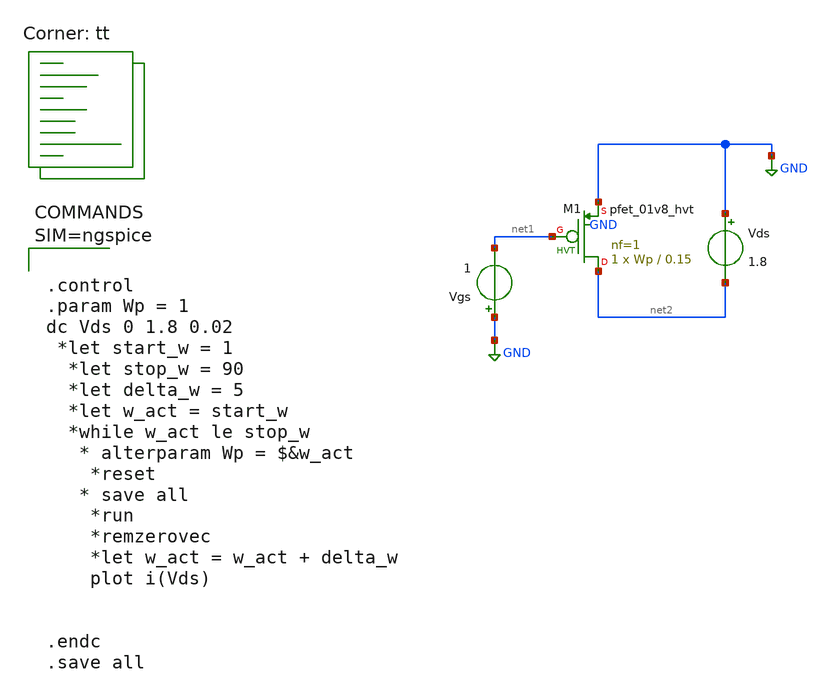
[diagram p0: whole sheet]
** sch_path: xschem/Polarizzazione0.sch
**.subckt Polarizzazione0
Vgs GND net1 1
Vds GND net2 1.8
XM1 net2 net1 GND GND sky130_fd_pr__pfet_01v8_hvt L=0.15 W=Wp nf=1 ad='int((nf+1)/2) * W/nf * 0.29' as='int((nf+2)/2) * W/nf * 0.29'
+ pd='2*int((nf+1)/2) * (W/nf + 0.29)' ps='2*int((nf+2)/2) * (W/nf + 0.29)' nrd='0.29 / W' nrs='0.29 / W'
+ sa=0 sb=0 sd=0 mult=1 m=1
**** begin user architecture code
.lib $::SKYWATER_MODELS/sky130.lib.spice tt



.control
.param Wp = 1
dc Vds 0 1.8 0.02
 *let start_w = 1
  *let stop_w = 90
  *let delta_w = 5
  *let w_act = start_w
  *while w_act le stop_w
   * alterparam Wp = $&w_act
    *reset
   * save all
    *run
    *remzerovec
    *let w_act = w_act + delta_w
    plot i(Vds)


.endc
.save all




**** end user architecture code
**.ends
.GLOBAL GND
.end
